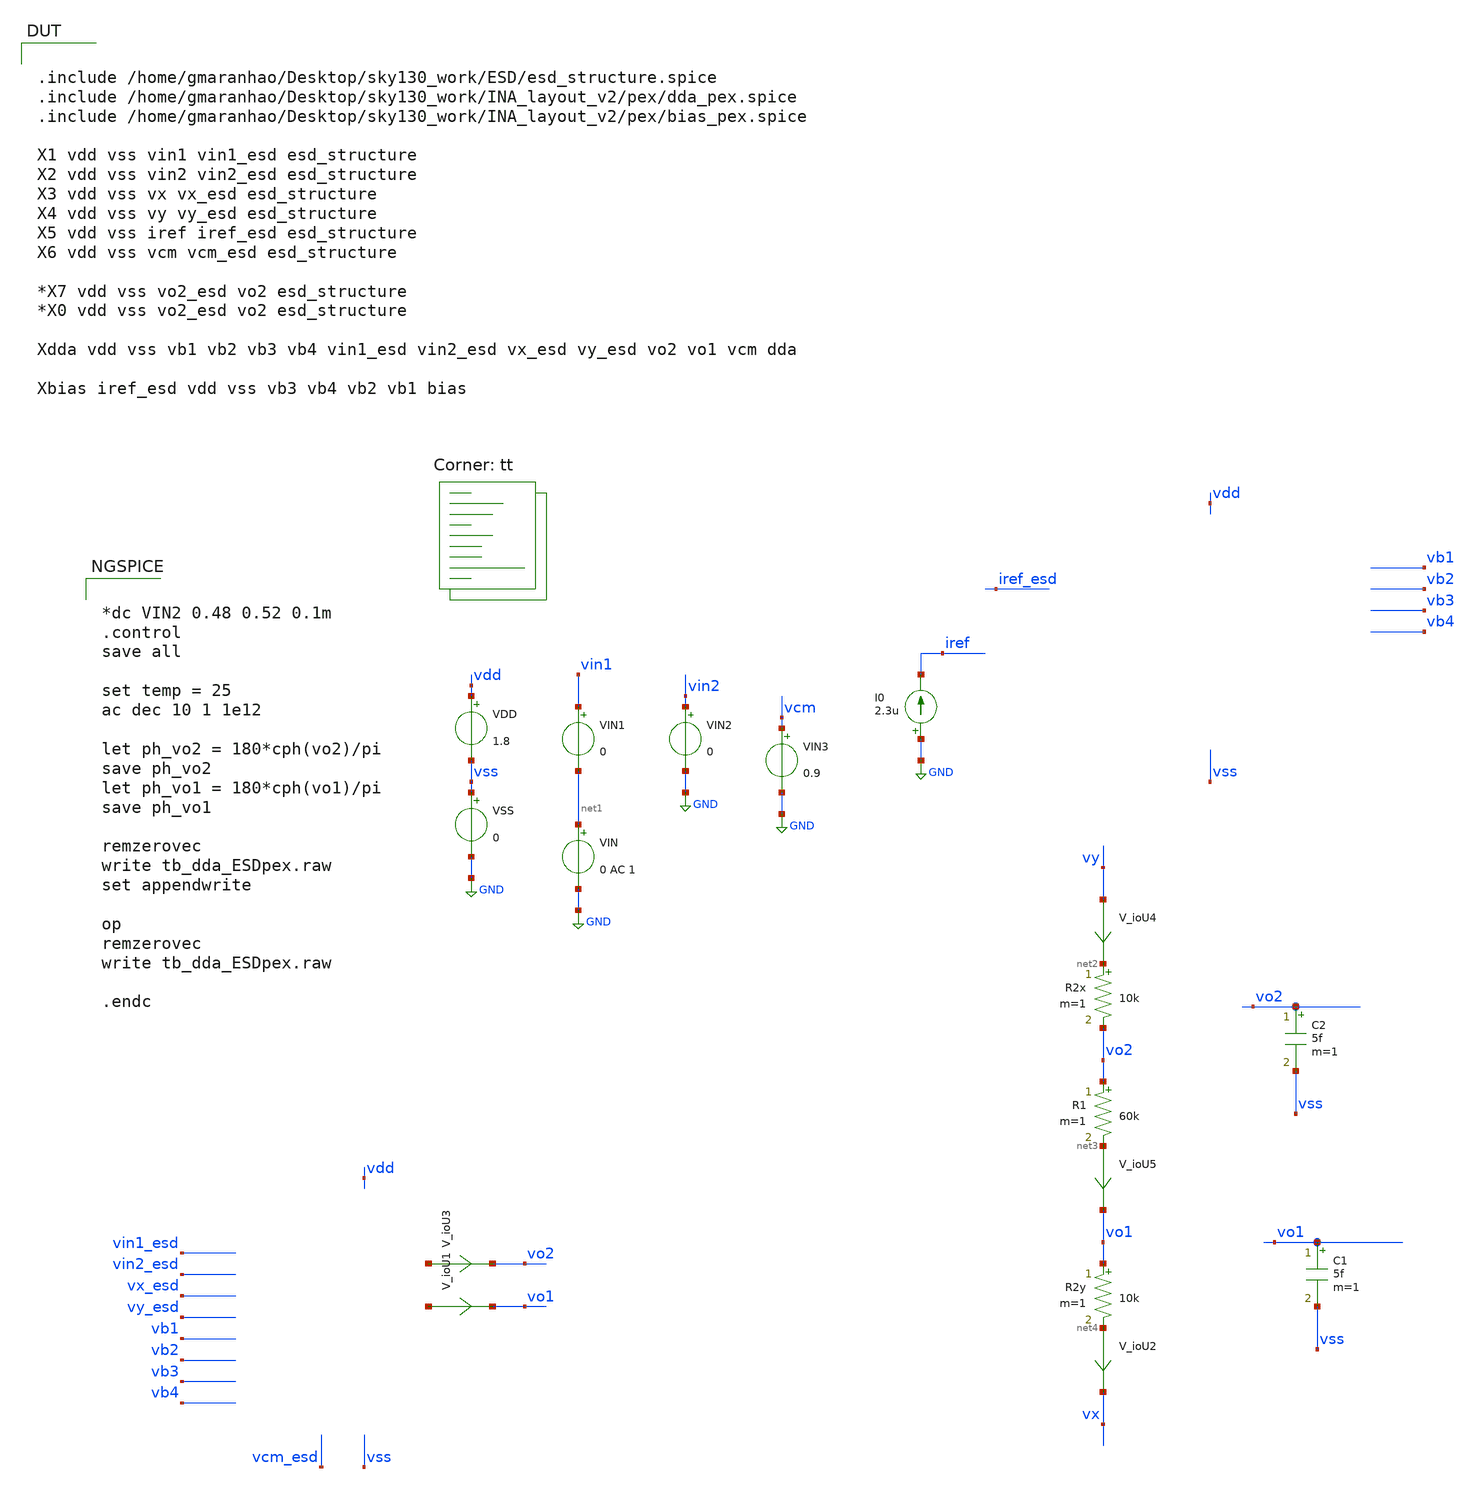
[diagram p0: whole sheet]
** sch_path: testbenches/tb_dda_ESDpex.sch
**.subckt tb_dda_ESDpex
VDD vdd vss 1.8
VSS vss GND 0
C1 vo1 vss 5f m=1
I0 GND iref 2.3u
VIN1 vin1 net1 0
VIN2 vin2 GND 0
VIN net1 GND 0 AC 1
C2 vo2 vss 5f m=1
VIN3 vcm GND 0.9
R2x net2 vo2 10k m=1
R1 vo2 net3 60k m=1
R2y vo1 net4 10k m=1
V_ioU3 net5 vo2 0
.save i(v_iou3)
V_ioU1 net6 vo1 0
.save i(v_iou1)
V_ioU2 net4 vx 0
.save i(v_iou2)
V_ioU4 vy net2 0
.save i(v_iou4)
V_ioU5 net3 vo1 0
.save i(v_iou5)
**** begin user architecture code


*dc VIN2 0.48 0.52 0.1m
.control
save all

set temp = 25
ac dec 10 1 1e12

let ph_vo2 = 180*cph(vo2)/pi
save ph_vo2
let ph_vo1 = 180*cph(vo1)/pi
save ph_vo1

remzerovec
write tb_dda_ESDpex.raw
set appendwrite

op
remzerovec
write tb_dda_ESDpex.raw

.endc


.lib $::SKYWATER_MODELS/sky130.lib.spice tt

.include /home/gmaranhao/Desktop/sky130_work/ESD/esd_structure.spice
.include /home/gmaranhao/Desktop/sky130_work/INA_layout_v2/pex/dda_pex.spice
.include /home/gmaranhao/Desktop/sky130_work/INA_layout_v2/pex/bias_pex.spice

X1 vdd vss vin1 vin1_esd esd_structure
X2 vdd vss vin2 vin2_esd esd_structure
X3 vdd vss vx vx_esd esd_structure
X4 vdd vss vy vy_esd esd_structure
X5 vdd vss iref iref_esd esd_structure
X6 vdd vss vcm vcm_esd esd_structure

*X7 vdd vss vo2_esd vo2 esd_structure
*X0 vdd vss vo2_esd vo2 esd_structure

Xdda vdd vss vb1 vb2 vb3 vb4 vin1_esd vin2_esd vx_esd vy_esd vo2 vo1 vcm dda

Xbias iref_esd vdd vss vb3 vb4 vb2 vb1 bias





**** end user architecture code
**.ends
.GLOBAL GND
.end
